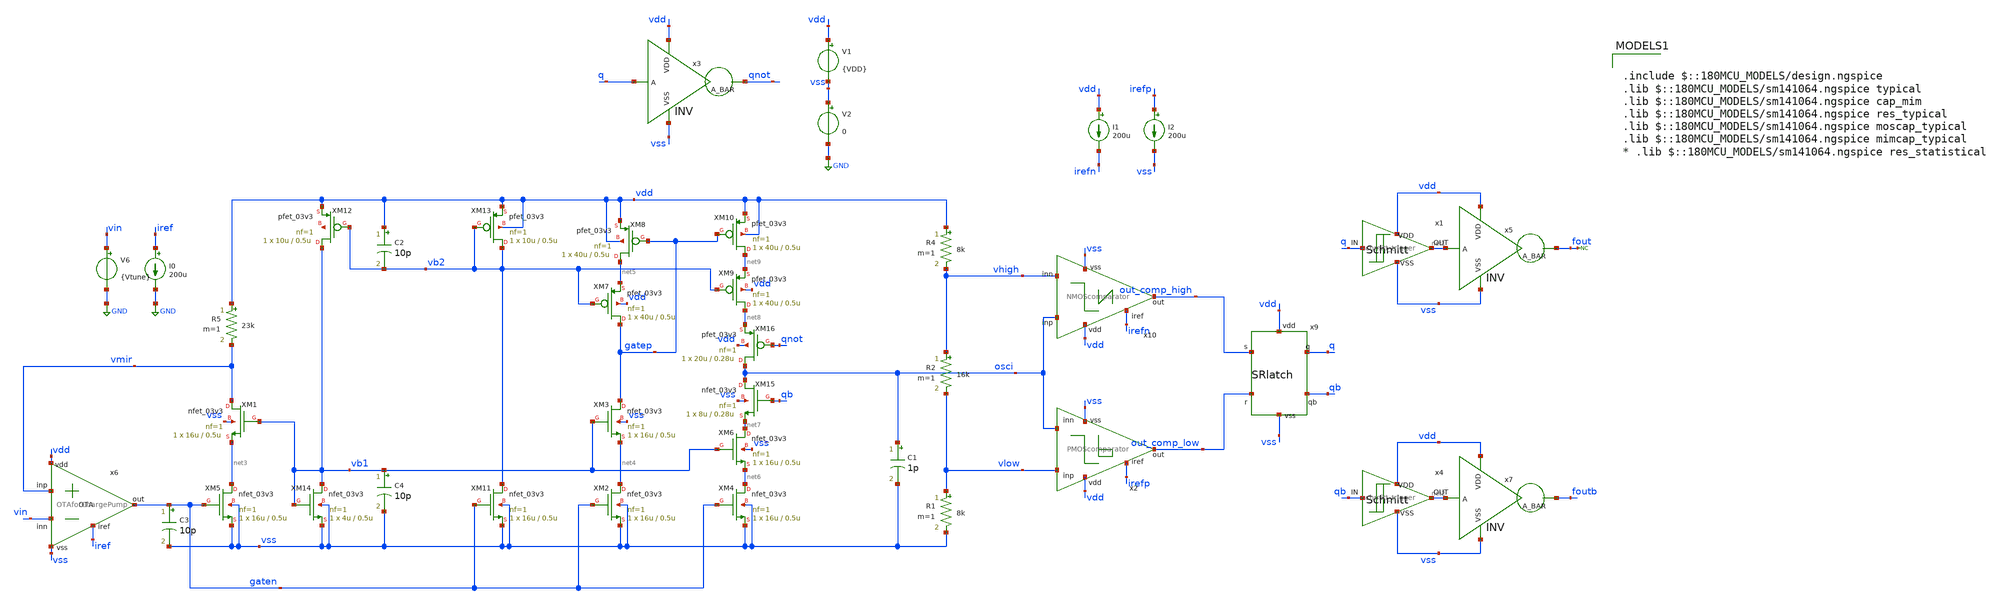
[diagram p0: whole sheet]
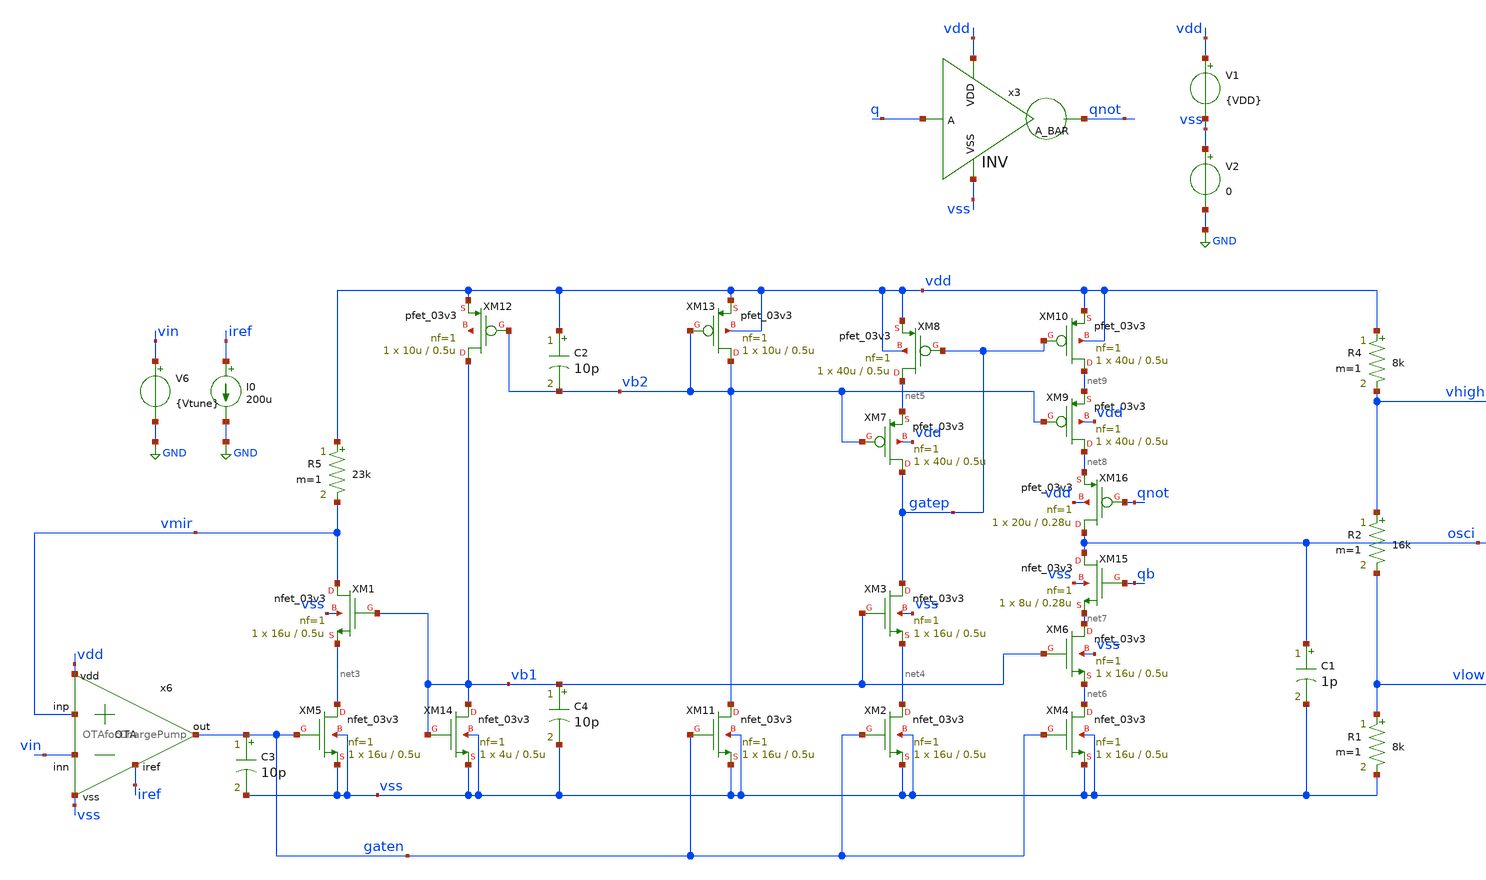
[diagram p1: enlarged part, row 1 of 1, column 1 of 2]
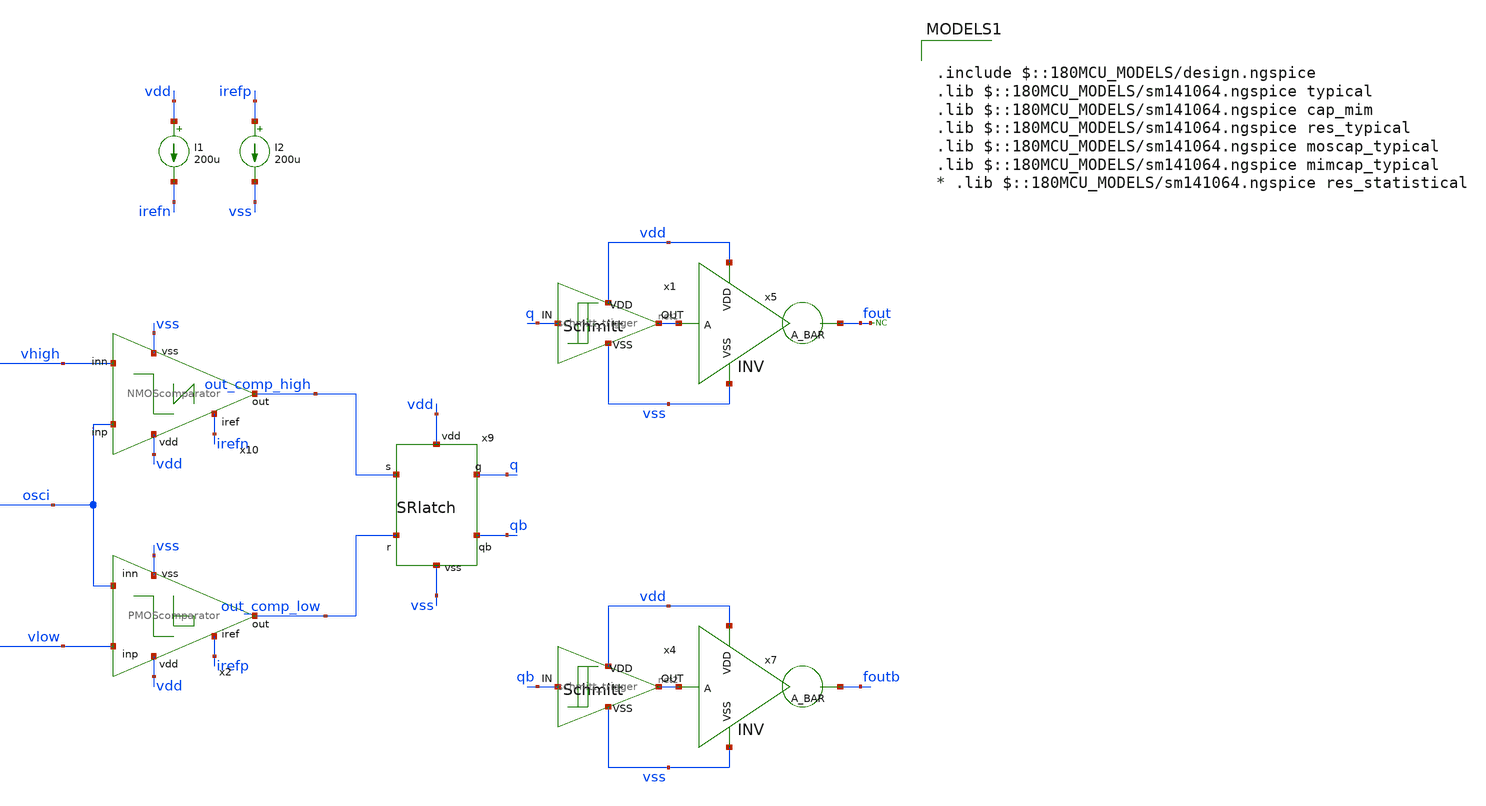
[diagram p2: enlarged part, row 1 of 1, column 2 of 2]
** sch_path: designs/libs/qw_core_analog_pkedit/qwedit_VCO/qwedit_VCO.sch
**.subckt qwedit_VCO
V1 vdd vss {VDD}
V2 vss GND 0
C1 osci vss 1p m=1
I1 vdd irefn 200u
I2 irefp vss 200u
R1 vlow vss 8k m=1
R2 vhigh vlow 16k m=1
R4 vdd vhigh 8k m=1
x9 vdd out_comp_high q qb out_comp_low vss SRlatch
x2 vdd irefp vlow out_comp_low osci vss PMOScomparator
x10 vdd osci out_comp_high vhigh irefn vss NMOScomparator
x3 vdd q qnot vss INV
x1 q net1 vdd vss schmitt_trigger
x4 qb net2 vdd vss schmitt_trigger
x5 vdd net1 fout vss INV
x7 vdd net2 foutb vss INV
x6 vdd iref vmir vin gaten vss OTAforChargePump
XM5 net3 gaten vss vss nfet_03v3 L=0.5u W=16u nf=1 ad='int((nf+1)/2) * W/nf * 0.18u' as='int((nf+2)/2) * W/nf * 0.18u'
+ pd='2*int((nf+1)/2) * (W/nf + 0.18u)' ps='2*int((nf+2)/2) * (W/nf + 0.18u)' nrd='0.18u / W' nrs='0.18u / W'
+ sa=0 sb=0 sd=0 m=1
XM1 vmir vb1 net3 vss nfet_03v3 L=0.5u W=16u nf=1 ad='int((nf+1)/2) * W/nf * 0.18u' as='int((nf+2)/2) * W/nf * 0.18u'
+ pd='2*int((nf+1)/2) * (W/nf + 0.18u)' ps='2*int((nf+2)/2) * (W/nf + 0.18u)' nrd='0.18u / W' nrs='0.18u / W'
+ sa=0 sb=0 sd=0 m=1
XM2 net4 gaten vss vss nfet_03v3 L=0.5u W=16u nf=1 ad='int((nf+1)/2) * W/nf * 0.18u' as='int((nf+2)/2) * W/nf * 0.18u'
+ pd='2*int((nf+1)/2) * (W/nf + 0.18u)' ps='2*int((nf+2)/2) * (W/nf + 0.18u)' nrd='0.18u / W' nrs='0.18u / W'
+ sa=0 sb=0 sd=0 m=1
XM3 gatep vb1 net4 vss nfet_03v3 L=0.5u W=16u nf=1 ad='int((nf+1)/2) * W/nf * 0.18u' as='int((nf+2)/2) * W/nf * 0.18u'
+ pd='2*int((nf+1)/2) * (W/nf + 0.18u)' ps='2*int((nf+2)/2) * (W/nf + 0.18u)' nrd='0.18u / W' nrs='0.18u / W'
+ sa=0 sb=0 sd=0 m=1
XM4 net6 gaten vss vss nfet_03v3 L=0.5u W=16u nf=1 ad='int((nf+1)/2) * W/nf * 0.18u' as='int((nf+2)/2) * W/nf * 0.18u'
+ pd='2*int((nf+1)/2) * (W/nf + 0.18u)' ps='2*int((nf+2)/2) * (W/nf + 0.18u)' nrd='0.18u / W' nrs='0.18u / W'
+ sa=0 sb=0 sd=0 m=1
XM6 net7 vb1 net6 vss nfet_03v3 L=0.5u W=16u nf=1 ad='int((nf+1)/2) * W/nf * 0.18u' as='int((nf+2)/2) * W/nf * 0.18u'
+ pd='2*int((nf+1)/2) * (W/nf + 0.18u)' ps='2*int((nf+2)/2) * (W/nf + 0.18u)' nrd='0.18u / W' nrs='0.18u / W'
+ sa=0 sb=0 sd=0 m=1
XM7 gatep vb2 net5 vdd pfet_03v3 L=0.5u W=40u nf=1 ad='int((nf+1)/2) * W/nf * 0.18u' as='int((nf+2)/2) * W/nf * 0.18u'
+ pd='2*int((nf+1)/2) * (W/nf + 0.18u)' ps='2*int((nf+2)/2) * (W/nf + 0.18u)' nrd='0.18u / W' nrs='0.18u / W'
+ sa=0 sb=0 sd=0 m=1
XM8 net5 gatep vdd vdd pfet_03v3 L=0.5u W=40u nf=1 ad='int((nf+1)/2) * W/nf * 0.18u' as='int((nf+2)/2) * W/nf * 0.18u'
+ pd='2*int((nf+1)/2) * (W/nf + 0.18u)' ps='2*int((nf+2)/2) * (W/nf + 0.18u)' nrd='0.18u / W' nrs='0.18u / W'
+ sa=0 sb=0 sd=0 m=1
XM9 net8 vb2 net9 vdd pfet_03v3 L=0.5u W=40u nf=1 ad='int((nf+1)/2) * W/nf * 0.18u' as='int((nf+2)/2) * W/nf * 0.18u'
+ pd='2*int((nf+1)/2) * (W/nf + 0.18u)' ps='2*int((nf+2)/2) * (W/nf + 0.18u)' nrd='0.18u / W' nrs='0.18u / W'
+ sa=0 sb=0 sd=0 m=1
XM10 net9 gatep vdd vdd pfet_03v3 L=0.5u W=40u nf=1 ad='int((nf+1)/2) * W/nf * 0.18u' as='int((nf+2)/2) * W/nf * 0.18u'
+ pd='2*int((nf+1)/2) * (W/nf + 0.18u)' ps='2*int((nf+2)/2) * (W/nf + 0.18u)' nrd='0.18u / W' nrs='0.18u / W'
+ sa=0 sb=0 sd=0 m=1
R5 vdd vmir 23k m=1
XM11 vb2 gaten vss vss nfet_03v3 L=0.5u W=16u nf=1 ad='int((nf+1)/2) * W/nf * 0.18u' as='int((nf+2)/2) * W/nf * 0.18u'
+ pd='2*int((nf+1)/2) * (W/nf + 0.18u)' ps='2*int((nf+2)/2) * (W/nf + 0.18u)' nrd='0.18u / W' nrs='0.18u / W'
+ sa=0 sb=0 sd=0 m=1
XM12 vb1 vb2 vdd net10 pfet_03v3 L=0.5u W=10u nf=1 ad='int((nf+1)/2) * W/nf * 0.18u' as='int((nf+2)/2) * W/nf * 0.18u'
+ pd='2*int((nf+1)/2) * (W/nf + 0.18u)' ps='2*int((nf+2)/2) * (W/nf + 0.18u)' nrd='0.18u / W' nrs='0.18u / W'
+ sa=0 sb=0 sd=0 m=1
XM13 vb2 vb2 vdd vdd pfet_03v3 L=0.5u W=10u nf=1 ad='int((nf+1)/2) * W/nf * 0.18u' as='int((nf+2)/2) * W/nf * 0.18u'
+ pd='2*int((nf+1)/2) * (W/nf + 0.18u)' ps='2*int((nf+2)/2) * (W/nf + 0.18u)' nrd='0.18u / W' nrs='0.18u / W'
+ sa=0 sb=0 sd=0 m=1
XM14 vb1 vb1 vss vss nfet_03v3 L=0.5u W=4u nf=1 ad='int((nf+1)/2) * W/nf * 0.18u' as='int((nf+2)/2) * W/nf * 0.18u'
+ pd='2*int((nf+1)/2) * (W/nf + 0.18u)' ps='2*int((nf+2)/2) * (W/nf + 0.18u)' nrd='0.18u / W' nrs='0.18u / W'
+ sa=0 sb=0 sd=0 m=1
XM15 osci qb net7 vss nfet_03v3 L=0.28u W=8u nf=1 ad='int((nf+1)/2) * W/nf * 0.18u' as='int((nf+2)/2) * W/nf * 0.18u'
+ pd='2*int((nf+1)/2) * (W/nf + 0.18u)' ps='2*int((nf+2)/2) * (W/nf + 0.18u)' nrd='0.18u / W' nrs='0.18u / W'
+ sa=0 sb=0 sd=0 m=1
XM16 osci qnot net8 vdd pfet_03v3 L=0.28u W=20u nf=1 ad='int((nf+1)/2) * W/nf * 0.18u' as='int((nf+2)/2) * W/nf * 0.18u'
+ pd='2*int((nf+1)/2) * (W/nf + 0.18u)' ps='2*int((nf+2)/2) * (W/nf + 0.18u)' nrd='0.18u / W' nrs='0.18u / W'
+ sa=0 sb=0 sd=0 m=1
V6 vin GND {Vtune}
I0 iref GND 200u
C3 gaten vss 10p m=1
* noconn fout
C2 vdd vb2 10p m=1
C4 vb1 vss 10p m=1
**** begin user architecture code


* .param par_vth=0 par_k=0 par_l=0 par_w=0 par_leff=0 par_weff=0 p_sqrtarea=0 var_k=0 var_vth=0
.param VDD = 3.3
.param Vtune = 0

.control
save all

**OP
**show all > op.log
**show all

** Source settings
alter @V1[PULSE] = [ 0 3.3 5n 1n 1n 49.998u 100u 0 ]

** Simulation settings
.step param Vtune 0 3.3 0.1
tran .1n 10u

.measure tran TPER TRIG fout VAL={VDD/2} RISE=1 FROM=5u  TARG fout VAL={VDD/2} RISE=2
.measure tran FREQ param='1/TPER'

write qwedit_VCO.raw
.endc



.include $::180MCU_MODELS/design.ngspice
.lib $::180MCU_MODELS/sm141064.ngspice typical
.lib $::180MCU_MODELS/sm141064.ngspice cap_mim
.lib $::180MCU_MODELS/sm141064.ngspice res_typical
.lib $::180MCU_MODELS/sm141064.ngspice moscap_typical
.lib $::180MCU_MODELS/sm141064.ngspice mimcap_typical
* .lib $::180MCU_MODELS/sm141064.ngspice res_statistical

**** end user architecture code
**.ends
.GLOBAL GND
.end
